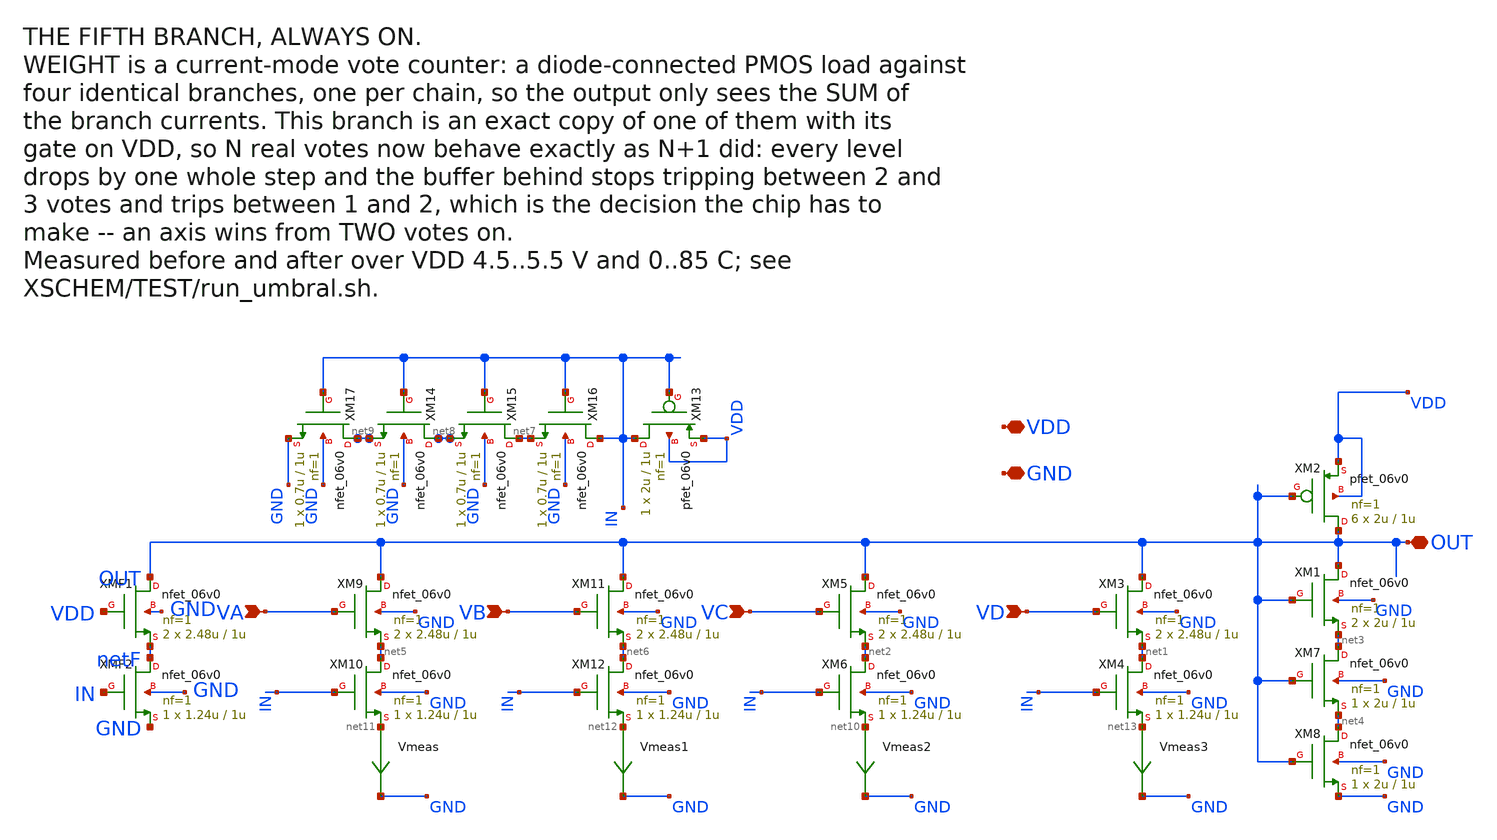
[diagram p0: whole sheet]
** sch_path: FINAL/XSCHEM/WEIGTH/WEIGHT.sch
**.subckt WEIGHT VDD GND VA VB VC VD OUT
*.iopin VDD
*.iopin GND
*.ipin VA
*.ipin VB
*.ipin VC
*.ipin VD
*.iopin OUT
XM2 OUT OUT VDD VDD pfet_06v0 L=1u W=2u nf=1 ad='int((nf+1)/2) * W/nf * 0.18u' as='int((nf+2)/2) * W/nf * 0.18u'
+ pd='2*int((nf+1)/2) * (W/nf + 0.18u)' ps='2*int((nf+2)/2) * (W/nf + 0.18u)' nrd='0.18u / W' nrs='0.18u / W'
+ sa=0 sb=0 sd=0 m=6
XM3 OUT VD net1 GND nfet_06v0 L=1u W=2.48u nf=1 ad='int((nf+1)/2) * W/nf * 0.18u' as='int((nf+2)/2) * W/nf * 0.18u'
+ pd='2*int((nf+1)/2) * (W/nf + 0.18u)' ps='2*int((nf+2)/2) * (W/nf + 0.18u)' nrd='0.18u / W' nrs='0.18u / W'
+ sa=0 sb=0 sd=0 m=2
XM5 OUT VC net2 GND nfet_06v0 L=1u W=2.48u nf=1 ad='int((nf+1)/2) * W/nf * 0.18u' as='int((nf+2)/2) * W/nf * 0.18u'
+ pd='2*int((nf+1)/2) * (W/nf + 0.18u)' ps='2*int((nf+2)/2) * (W/nf + 0.18u)' nrd='0.18u / W' nrs='0.18u / W'
+ sa=0 sb=0 sd=0 m=2
XM6 net2 IN net10 GND nfet_06v0 L=1u W=1.24u nf=1 ad='int((nf+1)/2) * W/nf * 0.18u' as='int((nf+2)/2) * W/nf * 0.18u'
+ pd='2*int((nf+1)/2) * (W/nf + 0.18u)' ps='2*int((nf+2)/2) * (W/nf + 0.18u)' nrd='0.18u / W' nrs='0.18u / W'
+ sa=0 sb=0 sd=0 m=1
XM1 OUT OUT net3 GND nfet_06v0 L=1u W=2u nf=1 ad='int((nf+1)/2) * W/nf * 0.18u' as='int((nf+2)/2) * W/nf * 0.18u'
+ pd='2*int((nf+1)/2) * (W/nf + 0.18u)' ps='2*int((nf+2)/2) * (W/nf + 0.18u)' nrd='0.18u / W' nrs='0.18u / W'
+ sa=0 sb=0 sd=0 m=2
XM7 net3 OUT net4 GND nfet_06v0 L=1u W=2u nf=1 ad='int((nf+1)/2) * W/nf * 0.18u' as='int((nf+2)/2) * W/nf * 0.18u'
+ pd='2*int((nf+1)/2) * (W/nf + 0.18u)' ps='2*int((nf+2)/2) * (W/nf + 0.18u)' nrd='0.18u / W' nrs='0.18u / W'
+ sa=0 sb=0 sd=0 m=1
XM8 net4 OUT GND GND nfet_06v0 L=1u W=2u nf=1 ad='int((nf+1)/2) * W/nf * 0.18u' as='int((nf+2)/2) * W/nf * 0.18u'
+ pd='2*int((nf+1)/2) * (W/nf + 0.18u)' ps='2*int((nf+2)/2) * (W/nf + 0.18u)' nrd='0.18u / W' nrs='0.18u / W'
+ sa=0 sb=0 sd=0 m=1
XM9 OUT VA net5 GND nfet_06v0 L=1u W=2.48u nf=1 ad='int((nf+1)/2) * W/nf * 0.18u' as='int((nf+2)/2) * W/nf * 0.18u'
+ pd='2*int((nf+1)/2) * (W/nf + 0.18u)' ps='2*int((nf+2)/2) * (W/nf + 0.18u)' nrd='0.18u / W' nrs='0.18u / W'
+ sa=0 sb=0 sd=0 m=2
XM10 net5 IN net11 GND nfet_06v0 L=1u W=1.24u nf=1 ad='int((nf+1)/2) * W/nf * 0.18u' as='int((nf+2)/2) * W/nf * 0.18u'
+ pd='2*int((nf+1)/2) * (W/nf + 0.18u)' ps='2*int((nf+2)/2) * (W/nf + 0.18u)' nrd='0.18u / W' nrs='0.18u / W'
+ sa=0 sb=0 sd=0 m=1
XM11 OUT VB net6 GND nfet_06v0 L=1u W=2.48u nf=1 ad='int((nf+1)/2) * W/nf * 0.18u' as='int((nf+2)/2) * W/nf * 0.18u'
+ pd='2*int((nf+1)/2) * (W/nf + 0.18u)' ps='2*int((nf+2)/2) * (W/nf + 0.18u)' nrd='0.18u / W' nrs='0.18u / W'
+ sa=0 sb=0 sd=0 m=2
XM12 net6 IN net12 GND nfet_06v0 L=1u W=1.24u nf=1 ad='int((nf+1)/2) * W/nf * 0.18u' as='int((nf+2)/2) * W/nf * 0.18u'
+ pd='2*int((nf+1)/2) * (W/nf + 0.18u)' ps='2*int((nf+2)/2) * (W/nf + 0.18u)' nrd='0.18u / W' nrs='0.18u / W'
+ sa=0 sb=0 sd=0 m=1
XM4 net1 IN net13 GND nfet_06v0 L=1u W=1.24u nf=1 ad='int((nf+1)/2) * W/nf * 0.18u' as='int((nf+2)/2) * W/nf * 0.18u'
+ pd='2*int((nf+1)/2) * (W/nf + 0.18u)' ps='2*int((nf+2)/2) * (W/nf + 0.18u)' nrd='0.18u / W' nrs='0.18u / W'
+ sa=0 sb=0 sd=0 m=1
XM13 IN IN VDD VDD pfet_06v0 L=1u W=2u nf=1 ad='int((nf+1)/2) * W/nf * 0.18u' as='int((nf+2)/2) * W/nf * 0.18u'
+ pd='2*int((nf+1)/2) * (W/nf + 0.18u)' ps='2*int((nf+2)/2) * (W/nf + 0.18u)' nrd='0.18u / W' nrs='0.18u / W'
+ sa=0 sb=0 sd=0 m=1
XM14 net8 IN net9 GND nfet_06v0 L=1u W=0.7u nf=1 ad='int((nf+1)/2) * W/nf * 0.18u' as='int((nf+2)/2) * W/nf * 0.18u'
+ pd='2*int((nf+1)/2) * (W/nf + 0.18u)' ps='2*int((nf+2)/2) * (W/nf + 0.18u)' nrd='0.18u / W' nrs='0.18u / W'
+ sa=0 sb=0 sd=0 m=1
XM15 net7 IN net8 GND nfet_06v0 L=1u W=0.7u nf=1 ad='int((nf+1)/2) * W/nf * 0.18u' as='int((nf+2)/2) * W/nf * 0.18u'
+ pd='2*int((nf+1)/2) * (W/nf + 0.18u)' ps='2*int((nf+2)/2) * (W/nf + 0.18u)' nrd='0.18u / W' nrs='0.18u / W'
+ sa=0 sb=0 sd=0 m=1
XM16 IN IN net7 GND nfet_06v0 L=1u W=0.7u nf=1 ad='int((nf+1)/2) * W/nf * 0.18u' as='int((nf+2)/2) * W/nf * 0.18u'
+ pd='2*int((nf+1)/2) * (W/nf + 0.18u)' ps='2*int((nf+2)/2) * (W/nf + 0.18u)' nrd='0.18u / W' nrs='0.18u / W'
+ sa=0 sb=0 sd=0 m=1
XM17 net9 IN GND GND nfet_06v0 L=1u W=0.7u nf=1 ad='int((nf+1)/2) * W/nf * 0.18u' as='int((nf+2)/2) * W/nf * 0.18u'
+ pd='2*int((nf+1)/2) * (W/nf + 0.18u)' ps='2*int((nf+2)/2) * (W/nf + 0.18u)' nrd='0.18u / W' nrs='0.18u / W'
+ sa=0 sb=0 sd=0 m=1
Vmeas net11 GND 0
.save i(vmeas)
Vmeas1 net12 GND 0
.save i(vmeas1)
Vmeas2 net10 GND 0
.save i(vmeas2)
Vmeas3 net13 GND 0
.save i(vmeas3)
XMF1 OUT VDD netF GND nfet_06v0 L=1u W=2.48u nf=1 ad='int((nf+1)/2) * W/nf * 0.18u' as='int((nf+2)/2) * W/nf * 0.18u'
+ pd='2*int((nf+1)/2) * (W/nf + 0.18u)' ps='2*int((nf+2)/2) * (W/nf + 0.18u)' nrd='0.18u / W' nrs='0.18u / W'
+ sa=0 sb=0 sd=0 m=2
XMF2 netF IN GND GND nfet_06v0 L=1u W=1.24u nf=1 ad='int((nf+1)/2) * W/nf * 0.18u' as='int((nf+2)/2) * W/nf * 0.18u'
+ pd='2*int((nf+1)/2) * (W/nf + 0.18u)' ps='2*int((nf+2)/2) * (W/nf + 0.18u)' nrd='0.18u / W' nrs='0.18u / W'
+ sa=0 sb=0 sd=0 m=1
**.ends
.end
